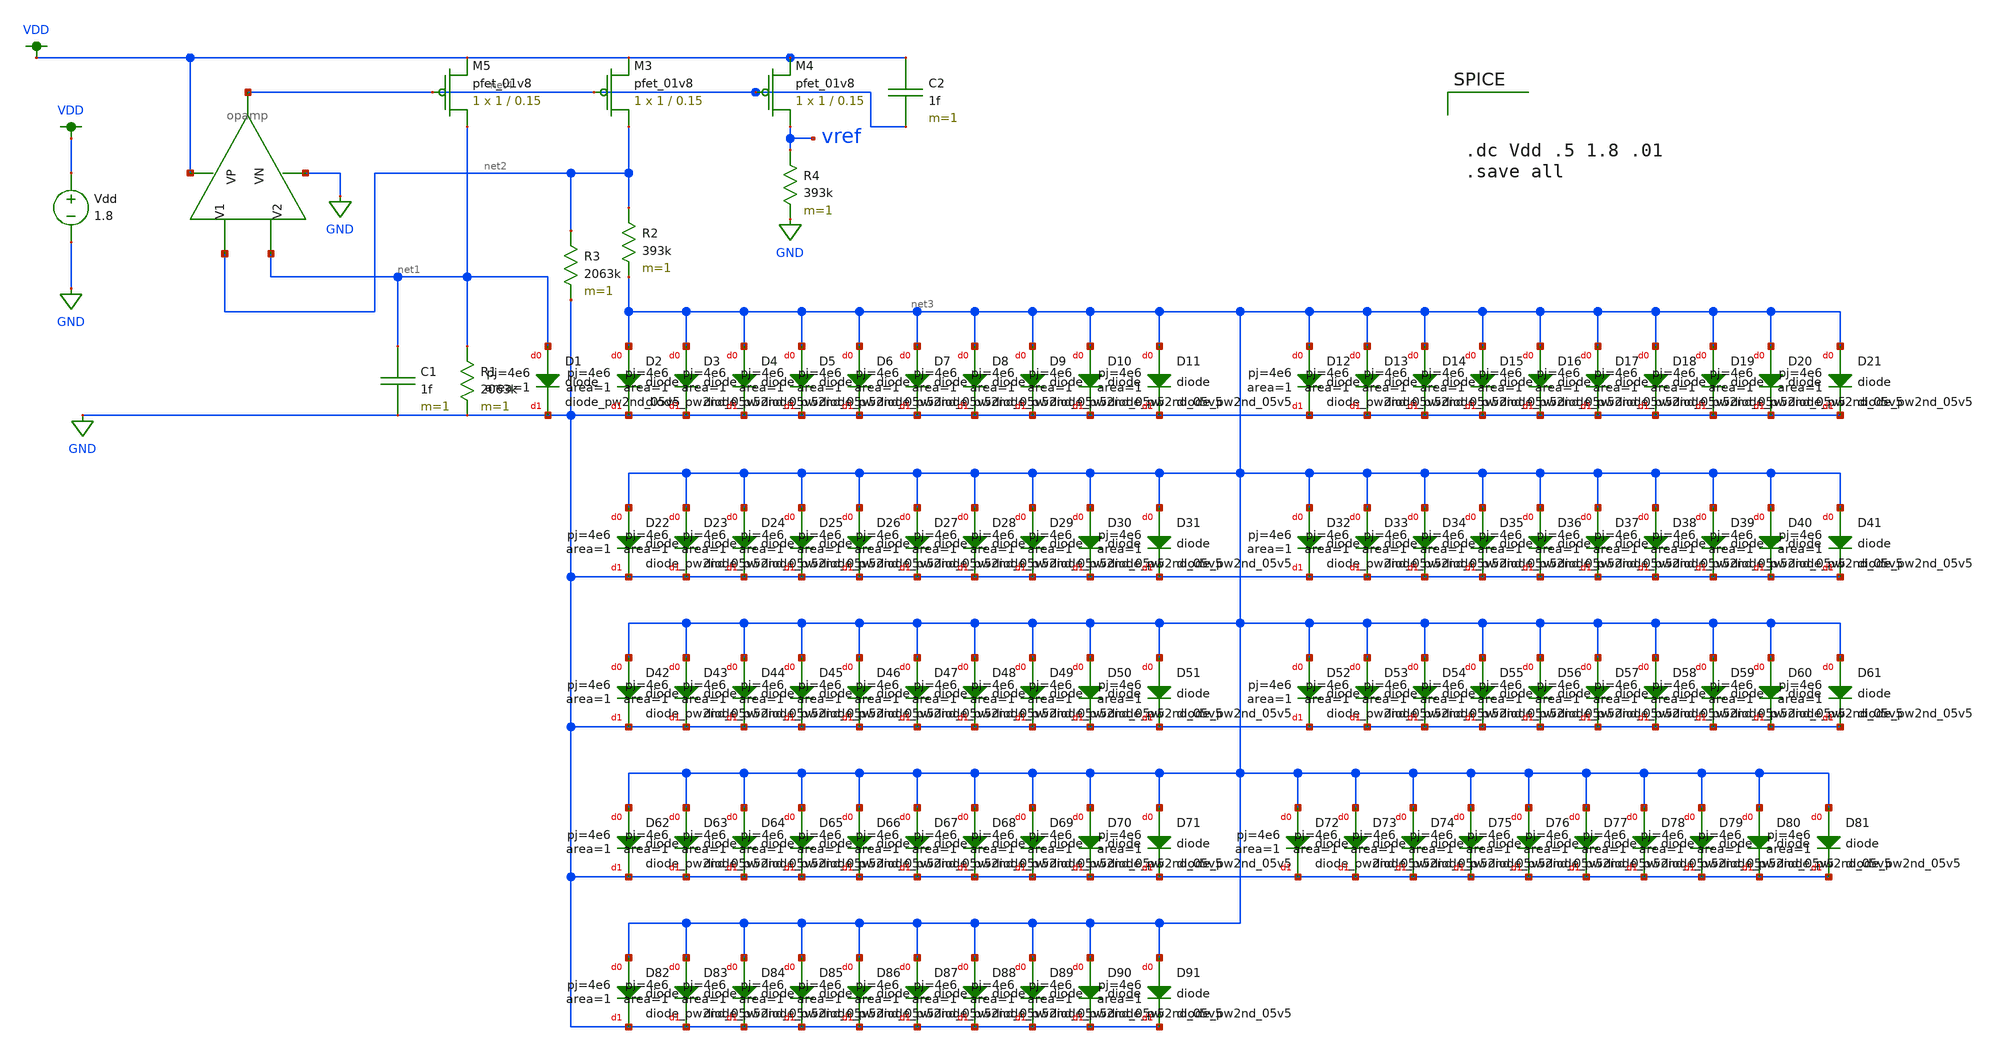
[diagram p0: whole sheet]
** sch_path: schematics/bandgap.sch
**.subckt bandgap
XD1 net1 GND sky130_fd_pr__diode_pw2nd_05v5 area=1 pj=4e6
XM4 vref net4 VDD VDD sky130_fd_pr__pfet_01v8 L=0.15 W=1 nf=1 ad='int((nf+1)/2) * W/nf * 0.29' as='int((nf+2)/2) * W/nf * 0.29'
+ pd='2*int((nf+1)/2) * (W/nf + 0.29)' ps='2*int((nf+2)/2) * (W/nf + 0.29)' nrd='0.29 / W' nrs='0.29 / W'
+ sa=0 sb=0 sd=0 mult=1 m=1
XM5 net1 net4 VDD VDD sky130_fd_pr__pfet_01v8 L=0.15 W=1 nf=1 ad='int((nf+1)/2) * W/nf * 0.29' as='int((nf+2)/2) * W/nf * 0.29'
+ pd='2*int((nf+1)/2) * (W/nf + 0.29)' ps='2*int((nf+2)/2) * (W/nf + 0.29)' nrd='0.29 / W' nrs='0.29 / W'
+ sa=0 sb=0 sd=0 mult=1 m=1
XM3 net2 net4 VDD VDD sky130_fd_pr__pfet_01v8 L=0.15 W=1 nf=1 ad='int((nf+1)/2) * W/nf * 0.29' as='int((nf+2)/2) * W/nf * 0.29'
+ pd='2*int((nf+1)/2) * (W/nf + 0.29)' ps='2*int((nf+2)/2) * (W/nf + 0.29)' nrd='0.29 / W' nrs='0.29 / W'
+ sa=0 sb=0 sd=0 mult=1 m=1
C1 net1 GND 1f m=1
R1 net1 GND 2063k m=1
XD2 net3 GND sky130_fd_pr__diode_pw2nd_05v5 area=1 pj=4e6
R2 net2 net3 393k m=1
XD3 net3 GND sky130_fd_pr__diode_pw2nd_05v5 area=1 pj=4e6
R3 net2 GND 2063k m=1
R4 vref GND 393k m=1
XD4 net3 GND sky130_fd_pr__diode_pw2nd_05v5 area=1 pj=4e6
XD5 net3 GND sky130_fd_pr__diode_pw2nd_05v5 area=1 pj=4e6
XD6 net3 GND sky130_fd_pr__diode_pw2nd_05v5 area=1 pj=4e6
XD7 net3 GND sky130_fd_pr__diode_pw2nd_05v5 area=1 pj=4e6
XD8 net3 GND sky130_fd_pr__diode_pw2nd_05v5 area=1 pj=4e6
XD9 net3 GND sky130_fd_pr__diode_pw2nd_05v5 area=1 pj=4e6
XD10 net3 GND sky130_fd_pr__diode_pw2nd_05v5 area=1 pj=4e6
XD11 net3 GND sky130_fd_pr__diode_pw2nd_05v5 area=1 pj=4e6
C2 VDD net4 1f m=1
Vdd VDD GND 1.8
X1 net2 net1 VDD GND net4 opamp
XD12 net3 GND sky130_fd_pr__diode_pw2nd_05v5 area=1 pj=4e6
XD13 net3 GND sky130_fd_pr__diode_pw2nd_05v5 area=1 pj=4e6
XD14 net3 GND sky130_fd_pr__diode_pw2nd_05v5 area=1 pj=4e6
XD15 net3 GND sky130_fd_pr__diode_pw2nd_05v5 area=1 pj=4e6
XD16 net3 GND sky130_fd_pr__diode_pw2nd_05v5 area=1 pj=4e6
XD17 net3 GND sky130_fd_pr__diode_pw2nd_05v5 area=1 pj=4e6
XD18 net3 GND sky130_fd_pr__diode_pw2nd_05v5 area=1 pj=4e6
XD19 net3 GND sky130_fd_pr__diode_pw2nd_05v5 area=1 pj=4e6
XD20 net3 GND sky130_fd_pr__diode_pw2nd_05v5 area=1 pj=4e6
XD21 net3 GND sky130_fd_pr__diode_pw2nd_05v5 area=1 pj=4e6
XD32 net3 GND sky130_fd_pr__diode_pw2nd_05v5 area=1 pj=4e6
XD33 net3 GND sky130_fd_pr__diode_pw2nd_05v5 area=1 pj=4e6
XD34 net3 GND sky130_fd_pr__diode_pw2nd_05v5 area=1 pj=4e6
XD35 net3 GND sky130_fd_pr__diode_pw2nd_05v5 area=1 pj=4e6
XD36 net3 GND sky130_fd_pr__diode_pw2nd_05v5 area=1 pj=4e6
XD37 net3 GND sky130_fd_pr__diode_pw2nd_05v5 area=1 pj=4e6
XD38 net3 GND sky130_fd_pr__diode_pw2nd_05v5 area=1 pj=4e6
XD39 net3 GND sky130_fd_pr__diode_pw2nd_05v5 area=1 pj=4e6
XD40 net3 GND sky130_fd_pr__diode_pw2nd_05v5 area=1 pj=4e6
XD41 net3 GND sky130_fd_pr__diode_pw2nd_05v5 area=1 pj=4e6
XD42 net3 GND sky130_fd_pr__diode_pw2nd_05v5 area=1 pj=4e6
XD43 net3 GND sky130_fd_pr__diode_pw2nd_05v5 area=1 pj=4e6
XD44 net3 GND sky130_fd_pr__diode_pw2nd_05v5 area=1 pj=4e6
XD45 net3 GND sky130_fd_pr__diode_pw2nd_05v5 area=1 pj=4e6
XD46 net3 GND sky130_fd_pr__diode_pw2nd_05v5 area=1 pj=4e6
XD47 net3 GND sky130_fd_pr__diode_pw2nd_05v5 area=1 pj=4e6
XD48 net3 GND sky130_fd_pr__diode_pw2nd_05v5 area=1 pj=4e6
XD49 net3 GND sky130_fd_pr__diode_pw2nd_05v5 area=1 pj=4e6
XD50 net3 GND sky130_fd_pr__diode_pw2nd_05v5 area=1 pj=4e6
XD51 net3 GND sky130_fd_pr__diode_pw2nd_05v5 area=1 pj=4e6
XD52 net3 GND sky130_fd_pr__diode_pw2nd_05v5 area=1 pj=4e6
XD53 net3 GND sky130_fd_pr__diode_pw2nd_05v5 area=1 pj=4e6
XD54 net3 GND sky130_fd_pr__diode_pw2nd_05v5 area=1 pj=4e6
XD55 net3 GND sky130_fd_pr__diode_pw2nd_05v5 area=1 pj=4e6
XD56 net3 GND sky130_fd_pr__diode_pw2nd_05v5 area=1 pj=4e6
XD57 net3 GND sky130_fd_pr__diode_pw2nd_05v5 area=1 pj=4e6
XD58 net3 GND sky130_fd_pr__diode_pw2nd_05v5 area=1 pj=4e6
XD59 net3 GND sky130_fd_pr__diode_pw2nd_05v5 area=1 pj=4e6
XD60 net3 GND sky130_fd_pr__diode_pw2nd_05v5 area=1 pj=4e6
XD61 net3 GND sky130_fd_pr__diode_pw2nd_05v5 area=1 pj=4e6
XD62 net3 GND sky130_fd_pr__diode_pw2nd_05v5 area=1 pj=4e6
XD63 net3 GND sky130_fd_pr__diode_pw2nd_05v5 area=1 pj=4e6
XD64 net3 GND sky130_fd_pr__diode_pw2nd_05v5 area=1 pj=4e6
XD65 net3 GND sky130_fd_pr__diode_pw2nd_05v5 area=1 pj=4e6
XD66 net3 GND sky130_fd_pr__diode_pw2nd_05v5 area=1 pj=4e6
XD67 net3 GND sky130_fd_pr__diode_pw2nd_05v5 area=1 pj=4e6
XD68 net3 GND sky130_fd_pr__diode_pw2nd_05v5 area=1 pj=4e6
XD69 net3 GND sky130_fd_pr__diode_pw2nd_05v5 area=1 pj=4e6
XD70 net3 GND sky130_fd_pr__diode_pw2nd_05v5 area=1 pj=4e6
XD71 net3 GND sky130_fd_pr__diode_pw2nd_05v5 area=1 pj=4e6
XD72 net3 GND sky130_fd_pr__diode_pw2nd_05v5 area=1 pj=4e6
XD73 net3 GND sky130_fd_pr__diode_pw2nd_05v5 area=1 pj=4e6
XD74 net3 GND sky130_fd_pr__diode_pw2nd_05v5 area=1 pj=4e6
XD75 net3 GND sky130_fd_pr__diode_pw2nd_05v5 area=1 pj=4e6
XD76 net3 GND sky130_fd_pr__diode_pw2nd_05v5 area=1 pj=4e6
XD77 net3 GND sky130_fd_pr__diode_pw2nd_05v5 area=1 pj=4e6
XD78 net3 GND sky130_fd_pr__diode_pw2nd_05v5 area=1 pj=4e6
XD79 net3 GND sky130_fd_pr__diode_pw2nd_05v5 area=1 pj=4e6
XD80 net3 GND sky130_fd_pr__diode_pw2nd_05v5 area=1 pj=4e6
XD81 net3 GND sky130_fd_pr__diode_pw2nd_05v5 area=1 pj=4e6
XD82 net3 GND sky130_fd_pr__diode_pw2nd_05v5 area=1 pj=4e6
XD83 net3 GND sky130_fd_pr__diode_pw2nd_05v5 area=1 pj=4e6
XD84 net3 GND sky130_fd_pr__diode_pw2nd_05v5 area=1 pj=4e6
XD85 net3 GND sky130_fd_pr__diode_pw2nd_05v5 area=1 pj=4e6
XD86 net3 GND sky130_fd_pr__diode_pw2nd_05v5 area=1 pj=4e6
XD87 net3 GND sky130_fd_pr__diode_pw2nd_05v5 area=1 pj=4e6
XD88 net3 GND sky130_fd_pr__diode_pw2nd_05v5 area=1 pj=4e6
XD89 net3 GND sky130_fd_pr__diode_pw2nd_05v5 area=1 pj=4e6
XD90 net3 GND sky130_fd_pr__diode_pw2nd_05v5 area=1 pj=4e6
XD91 net3 GND sky130_fd_pr__diode_pw2nd_05v5 area=1 pj=4e6
XD22 net3 GND sky130_fd_pr__diode_pw2nd_05v5 area=1 pj=4e6
XD23 net3 GND sky130_fd_pr__diode_pw2nd_05v5 area=1 pj=4e6
XD24 net3 GND sky130_fd_pr__diode_pw2nd_05v5 area=1 pj=4e6
XD25 net3 GND sky130_fd_pr__diode_pw2nd_05v5 area=1 pj=4e6
XD26 net3 GND sky130_fd_pr__diode_pw2nd_05v5 area=1 pj=4e6
XD27 net3 GND sky130_fd_pr__diode_pw2nd_05v5 area=1 pj=4e6
XD28 net3 GND sky130_fd_pr__diode_pw2nd_05v5 area=1 pj=4e6
XD29 net3 GND sky130_fd_pr__diode_pw2nd_05v5 area=1 pj=4e6
XD30 net3 GND sky130_fd_pr__diode_pw2nd_05v5 area=1 pj=4e6
XD31 net3 GND sky130_fd_pr__diode_pw2nd_05v5 area=1 pj=4e6
**** begin user architecture code

.option wnflag=1
.param MC_SWITCH=0.0
.lib ~/skywater/skywater-pdk/libraries/sky130_fd_pr_ngspice/latest/models/sky130.lib.spice tt




.dc Vdd .5 1.8 .01
.save all


**** end user architecture code
**.ends

* expanding   symbol:  /home/madvlsi/Desktop/MADVLSI_final/schematics/opamp.sym # of pins=5
** sym_path: schematics/opamp.sym
** sch_path: schematics/opamp.sch
.subckt opamp V1 V2 VP VN Vout
*.ipin V1
*.ipin V2
*.opin Vout
*.iopin VP
*.iopin VN
*.iopin VP
*.iopin VN
XM1 VN net7 net2 GND sky130_fd_pr__nfet_01v8 L=l W=w nf=1 ad='int((nf+1)/2) * W/nf * 0.29' as='int((nf+2)/2) * W/nf * 0.29'
+ pd='2*int((nf+1)/2) * (W/nf + 0.29)' ps='2*int((nf+2)/2) * (W/nf + 0.29)' nrd='0.29 / W' nrs='0.29 / W'
+ sa=0 sb=0 sd=0 mult=1 m=1
XM2 VP net3 net1 VDD sky130_fd_pr__pfet_01v8 L=l W=w nf=1 ad='int((nf+1)/2) * W/nf * 0.29' as='int((nf+2)/2) * W/nf * 0.29'
+ pd='2*int((nf+1)/2) * (W/nf + 0.29)' ps='2*int((nf+2)/2) * (W/nf + 0.29)' nrd='0.29 / W' nrs='0.29 / W'
+ sa=0 sb=0 sd=0 mult=1 m=1
XM3 net1 V1 Vd VDD sky130_fd_pr__pfet_01v8 L=l W=w nf=1 ad='int((nf+1)/2) * W/nf * 0.29' as='int((nf+2)/2) * W/nf * 0.29'
+ pd='2*int((nf+1)/2) * (W/nf + 0.29)' ps='2*int((nf+2)/2) * (W/nf + 0.29)' nrd='0.29 / W' nrs='0.29 / W'
+ sa=0 sb=0 sd=0 mult=1 m=1
XM4 Vc V2 net1 VDD sky130_fd_pr__pfet_01v8 L=l W=w nf=1 ad='int((nf+1)/2) * W/nf * 0.29' as='int((nf+2)/2) * W/nf * 0.29'
+ pd='2*int((nf+1)/2) * (W/nf + 0.29)' ps='2*int((nf+2)/2) * (W/nf + 0.29)' nrd='0.29 / W' nrs='0.29 / W'
+ sa=0 sb=0 sd=0 mult=1 m=1
XM5 Va V2 net2 GND sky130_fd_pr__nfet_01v8 L=l W=w nf=1 ad='int((nf+1)/2) * W/nf * 0.29' as='int((nf+2)/2) * W/nf * 0.29'
+ pd='2*int((nf+1)/2) * (W/nf + 0.29)' ps='2*int((nf+2)/2) * (W/nf + 0.29)' nrd='0.29 / W' nrs='0.29 / W'
+ sa=0 sb=0 sd=0 mult=1 m=1
XM6 net2 V1 Vb GND sky130_fd_pr__nfet_01v8 L=l W=w nf=1 ad='int((nf+1)/2) * W/nf * 0.29' as='int((nf+2)/2) * W/nf * 0.29'
+ pd='2*int((nf+1)/2) * (W/nf + 0.29)' ps='2*int((nf+2)/2) * (W/nf + 0.29)' nrd='0.29 / W' nrs='0.29 / W'
+ sa=0 sb=0 sd=0 mult=1 m=1
XM7 net3 net3 Va VDD sky130_fd_pr__pfet_01v8 L=l W=w nf=1 ad='int((nf+1)/2) * W/nf * 0.29' as='int((nf+2)/2) * W/nf * 0.29'
+ pd='2*int((nf+1)/2) * (W/nf + 0.29)' ps='2*int((nf+2)/2) * (W/nf + 0.29)' nrd='0.29 / W' nrs='0.29 / W'
+ sa=0 sb=0 sd=0 mult=1 m=1
XM8 net6 net6 Va VDD sky130_fd_pr__pfet_01v8 L=l W=w nf=1 ad='int((nf+1)/2) * W/nf * 0.29' as='int((nf+2)/2) * W/nf * 0.29'
+ pd='2*int((nf+1)/2) * (W/nf + 0.29)' ps='2*int((nf+2)/2) * (W/nf + 0.29)' nrd='0.29 / W' nrs='0.29 / W'
+ sa=0 sb=0 sd=0 mult=1 m=1
XM9 net5 net6 Vb VDD sky130_fd_pr__pfet_01v8 L=l W=w nf=1 ad='int((nf+1)/2) * W/nf * 0.29' as='int((nf+2)/2) * W/nf * 0.29'
+ pd='2*int((nf+1)/2) * (W/nf + 0.29)' ps='2*int((nf+2)/2) * (W/nf + 0.29)' nrd='0.29 / W' nrs='0.29 / W'
+ sa=0 sb=0 sd=0 mult=1 m=1
XM10 Va net3 VP VDD sky130_fd_pr__pfet_01v8 L=l W=w nf=1 ad='int((nf+1)/2) * W/nf * 0.29' as='int((nf+2)/2) * W/nf * 0.29'
+ pd='2*int((nf+1)/2) * (W/nf + 0.29)' ps='2*int((nf+2)/2) * (W/nf + 0.29)' nrd='0.29 / W' nrs='0.29 / W'
+ sa=0 sb=0 sd=0 mult=1 m=1
XM11 Vb net3 VP VDD sky130_fd_pr__pfet_01v8 L=l W=w nf=1 ad='int((nf+1)/2) * W/nf * 0.29' as='int((nf+2)/2) * W/nf * 0.29'
+ pd='2*int((nf+1)/2) * (W/nf + 0.29)' ps='2*int((nf+2)/2) * (W/nf + 0.29)' nrd='0.29 / W' nrs='0.29 / W'
+ sa=0 sb=0 sd=0 mult=1 m=1
XM12 net6 net6 Vc GND sky130_fd_pr__nfet_01v8 L=l W=w nf=1 ad='int((nf+1)/2) * W/nf * 0.29' as='int((nf+2)/2) * W/nf * 0.29'
+ pd='2*int((nf+1)/2) * (W/nf + 0.29)' ps='2*int((nf+2)/2) * (W/nf + 0.29)' nrd='0.29 / W' nrs='0.29 / W'
+ sa=0 sb=0 sd=0 mult=1 m=1
XM13 net5 net6 Vd GND sky130_fd_pr__nfet_01v8 L=l W=w nf=1 ad='int((nf+1)/2) * W/nf * 0.29' as='int((nf+2)/2) * W/nf * 0.29'
+ pd='2*int((nf+1)/2) * (W/nf + 0.29)' ps='2*int((nf+2)/2) * (W/nf + 0.29)' nrd='0.29 / W' nrs='0.29 / W'
+ sa=0 sb=0 sd=0 mult=1 m=1
XM14 Vc net7 VN GND sky130_fd_pr__nfet_01v8 L=l W=w nf=1 ad='int((nf+1)/2) * W/nf * 0.29' as='int((nf+2)/2) * W/nf * 0.29'
+ pd='2*int((nf+1)/2) * (W/nf + 0.29)' ps='2*int((nf+2)/2) * (W/nf + 0.29)' nrd='0.29 / W' nrs='0.29 / W'
+ sa=0 sb=0 sd=0 mult=1 m=1
XM15 Vd net7 VN GND sky130_fd_pr__nfet_01v8 L=l W=w nf=1 ad='int((nf+1)/2) * W/nf * 0.29' as='int((nf+2)/2) * W/nf * 0.29'
+ pd='2*int((nf+1)/2) * (W/nf + 0.29)' ps='2*int((nf+2)/2) * (W/nf + 0.29)' nrd='0.29 / W' nrs='0.29 / W'
+ sa=0 sb=0 sd=0 mult=1 m=1
XM16 net8 net7 net3 GND sky130_fd_pr__nfet_01v8 L=l W=w nf=1 ad='int((nf+1)/2) * W/nf * 0.29' as='int((nf+2)/2) * W/nf * 0.29'
+ pd='2*int((nf+1)/2) * (W/nf + 0.29)' ps='2*int((nf+2)/2) * (W/nf + 0.29)' nrd='0.29 / W' nrs='0.29 / W'
+ sa=0 sb=0 sd=0 mult=1 m=1
XM17 VN net7 net8 GND sky130_fd_pr__nfet_01v8 L=l W=w nf=1 ad='int((nf+1)/2) * W/nf * 0.29' as='int((nf+2)/2) * W/nf * 0.29'
+ pd='2*int((nf+1)/2) * (W/nf + 0.29)' ps='2*int((nf+2)/2) * (W/nf + 0.29)' nrd='0.29 / W' nrs='0.29 / W'
+ sa=0 sb=0 sd=0 mult=1 m=1
XM18 net8 net7 VP GND sky130_fd_pr__nfet_01v8 L=l W=w nf=1 ad='int((nf+1)/2) * W/nf * 0.29' as='int((nf+2)/2) * W/nf * 0.29'
+ pd='2*int((nf+1)/2) * (W/nf + 0.29)' ps='2*int((nf+2)/2) * (W/nf + 0.29)' nrd='0.29 / W' nrs='0.29 / W'
+ sa=0 sb=0 sd=0 mult=M m=M
XM19 net4 net3 net7 VDD sky130_fd_pr__pfet_01v8 L=l W=w nf=1 ad='int((nf+1)/2) * W/nf * 0.29' as='int((nf+2)/2) * W/nf * 0.29'
+ pd='2*int((nf+1)/2) * (W/nf + 0.29)' ps='2*int((nf+2)/2) * (W/nf + 0.29)' nrd='0.29 / W' nrs='0.29 / W'
+ sa=0 sb=0 sd=0 mult=1 m=1
XM20 VP net3 net4 VDD sky130_fd_pr__pfet_01v8 L=l W=w nf=1 ad='int((nf+1)/2) * W/nf * 0.29' as='int((nf+2)/2) * W/nf * 0.29'
+ pd='2*int((nf+1)/2) * (W/nf + 0.29)' ps='2*int((nf+2)/2) * (W/nf + 0.29)' nrd='0.29 / W' nrs='0.29 / W'
+ sa=0 sb=0 sd=0 mult=1 m=1
XM21 net4 net3 VN VDD sky130_fd_pr__pfet_01v8 L=l W=w nf=1 ad='int((nf+1)/2) * W/nf * 0.29' as='int((nf+2)/2) * W/nf * 0.29'
+ pd='2*int((nf+1)/2) * (W/nf + 0.29)' ps='2*int((nf+2)/2) * (W/nf + 0.29)' nrd='0.29 / W' nrs='0.29 / W'
+ sa=0 sb=0 sd=0 mult=M m=M
XM22 net7 net7 Vc GND sky130_fd_pr__nfet_01v8 L=l W=w nf=1 ad='int((nf+1)/2) * W/nf * 0.29' as='int((nf+2)/2) * W/nf * 0.29'
+ pd='2*int((nf+1)/2) * (W/nf + 0.29)' ps='2*int((nf+2)/2) * (W/nf + 0.29)' nrd='0.29 / W' nrs='0.29 / W'
+ sa=0 sb=0 sd=0 mult=1 m=1
**** begin user architecture code

.param M=3
.param w=3
.param l=0.6


**** end user architecture code
XM23 Vout net5 VN GND sky130_fd_pr__nfet_01v8 L=.15 W=6 nf=1 ad='int((nf+1)/2) * W/nf * 0.29' as='int((nf+2)/2) * W/nf * 0.29'
+ pd='2*int((nf+1)/2) * (W/nf + 0.29)' ps='2*int((nf+2)/2) * (W/nf + 0.29)' nrd='0.29 / W' nrs='0.29 / W'
+ sa=0 sb=0 sd=0 mult=1 m=1
XM24 Vout net5 VP VDD sky130_fd_pr__pfet_01v8 L=.15 W=12 nf=1 ad='int((nf+1)/2) * W/nf * 0.29' as='int((nf+2)/2) * W/nf * 0.29'
+ pd='2*int((nf+1)/2) * (W/nf + 0.29)' ps='2*int((nf+2)/2) * (W/nf + 0.29)' nrd='0.29 / W' nrs='0.29 / W'
+ sa=0 sb=0 sd=0 mult=1 m=1
C1 Vout net5 500f m=1
.ends

.GLOBAL VDD
.GLOBAL GND
.end
